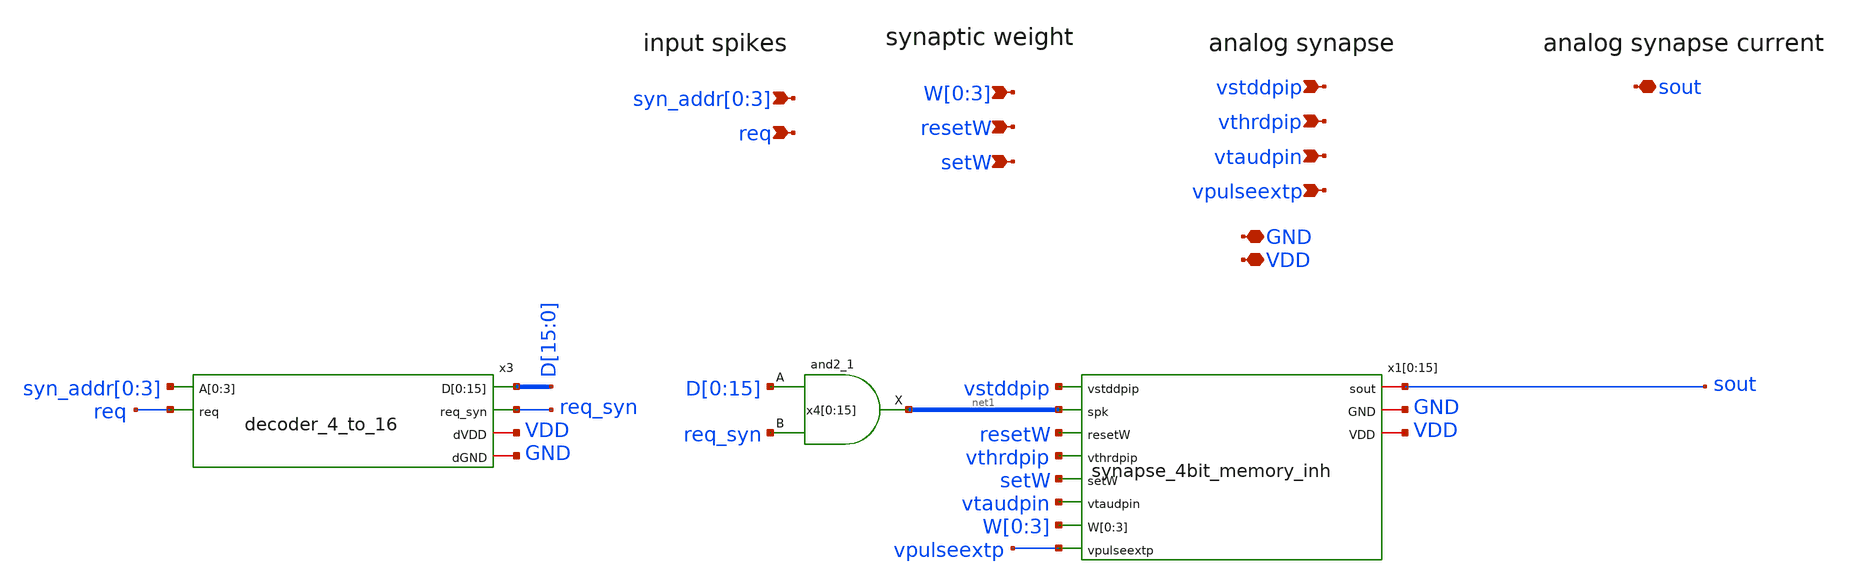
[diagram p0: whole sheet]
** sch_path: design/xschem/synapse_array_programmable_inh_16_to_sout.sch
**.subckt synapse_array_programmable_inh_16_to_sout GND VDD vpulseextp
*+ syn_addr[0],syn_addr[1],syn_addr[2],syn_addr[3] W[0],W[1],W[2],W[3] vthrdpip vtaudpin vstddpip sout setW resetW req
*.iopin GND
*.iopin VDD
*.ipin vpulseextp
*.ipin syn_addr[0],syn_addr[1],syn_addr[2],syn_addr[3]
*.ipin W[0],W[1],W[2],W[3]
*.ipin vthrdpip
*.ipin vtaudpin
*.ipin vstddpip
*.iopin sout
*.ipin setW
*.ipin resetW
*.ipin req
x3 syn_addr[0] syn_addr[1] syn_addr[2] syn_addr[3] D[15] D[14] D[13] D[12] D[11] D[10] D[9] D[8]
+ D[7] D[6] D[5] D[4] D[3] D[2] D[1] D[0] req req_syn VDD GND decoder_4_to_16
x4[0] D[0] req_syn GND GND VDD VDD net1[15] sky130_fd_sc_hd__and2_1
x4[1] D[1] req_syn GND GND VDD VDD net1[14] sky130_fd_sc_hd__and2_1
x4[2] D[2] req_syn GND GND VDD VDD net1[13] sky130_fd_sc_hd__and2_1
x4[3] D[3] req_syn GND GND VDD VDD net1[12] sky130_fd_sc_hd__and2_1
x4[4] D[4] req_syn GND GND VDD VDD net1[11] sky130_fd_sc_hd__and2_1
x4[5] D[5] req_syn GND GND VDD VDD net1[10] sky130_fd_sc_hd__and2_1
x4[6] D[6] req_syn GND GND VDD VDD net1[9] sky130_fd_sc_hd__and2_1
x4[7] D[7] req_syn GND GND VDD VDD net1[8] sky130_fd_sc_hd__and2_1
x4[8] D[8] req_syn GND GND VDD VDD net1[7] sky130_fd_sc_hd__and2_1
x4[9] D[9] req_syn GND GND VDD VDD net1[6] sky130_fd_sc_hd__and2_1
x4[10] D[10] req_syn GND GND VDD VDD net1[5] sky130_fd_sc_hd__and2_1
x4[11] D[11] req_syn GND GND VDD VDD net1[4] sky130_fd_sc_hd__and2_1
x4[12] D[12] req_syn GND GND VDD VDD net1[3] sky130_fd_sc_hd__and2_1
x4[13] D[13] req_syn GND GND VDD VDD net1[2] sky130_fd_sc_hd__and2_1
x4[14] D[14] req_syn GND GND VDD VDD net1[1] sky130_fd_sc_hd__and2_1
x4[15] D[15] req_syn GND GND VDD VDD net1[0] sky130_fd_sc_hd__and2_1
x1[0] sout vstddpip net1[15] resetW vthrdpip setW vtaudpin W[0] W[1] W[2] W[3] vpulseextp GND VDD
+ synapse_4bit_memory_inh
x1[1] sout vstddpip net1[14] resetW vthrdpip setW vtaudpin W[0] W[1] W[2] W[3] vpulseextp GND VDD
+ synapse_4bit_memory_inh
x1[2] sout vstddpip net1[13] resetW vthrdpip setW vtaudpin W[0] W[1] W[2] W[3] vpulseextp GND VDD
+ synapse_4bit_memory_inh
x1[3] sout vstddpip net1[12] resetW vthrdpip setW vtaudpin W[0] W[1] W[2] W[3] vpulseextp GND VDD
+ synapse_4bit_memory_inh
x1[4] sout vstddpip net1[11] resetW vthrdpip setW vtaudpin W[0] W[1] W[2] W[3] vpulseextp GND VDD
+ synapse_4bit_memory_inh
x1[5] sout vstddpip net1[10] resetW vthrdpip setW vtaudpin W[0] W[1] W[2] W[3] vpulseextp GND VDD
+ synapse_4bit_memory_inh
x1[6] sout vstddpip net1[9] resetW vthrdpip setW vtaudpin W[0] W[1] W[2] W[3] vpulseextp GND VDD
+ synapse_4bit_memory_inh
x1[7] sout vstddpip net1[8] resetW vthrdpip setW vtaudpin W[0] W[1] W[2] W[3] vpulseextp GND VDD
+ synapse_4bit_memory_inh
x1[8] sout vstddpip net1[7] resetW vthrdpip setW vtaudpin W[0] W[1] W[2] W[3] vpulseextp GND VDD
+ synapse_4bit_memory_inh
x1[9] sout vstddpip net1[6] resetW vthrdpip setW vtaudpin W[0] W[1] W[2] W[3] vpulseextp GND VDD
+ synapse_4bit_memory_inh
x1[10] sout vstddpip net1[5] resetW vthrdpip setW vtaudpin W[0] W[1] W[2] W[3] vpulseextp GND VDD
+ synapse_4bit_memory_inh
x1[11] sout vstddpip net1[4] resetW vthrdpip setW vtaudpin W[0] W[1] W[2] W[3] vpulseextp GND VDD
+ synapse_4bit_memory_inh
x1[12] sout vstddpip net1[3] resetW vthrdpip setW vtaudpin W[0] W[1] W[2] W[3] vpulseextp GND VDD
+ synapse_4bit_memory_inh
x1[13] sout vstddpip net1[2] resetW vthrdpip setW vtaudpin W[0] W[1] W[2] W[3] vpulseextp GND VDD
+ synapse_4bit_memory_inh
x1[14] sout vstddpip net1[1] resetW vthrdpip setW vtaudpin W[0] W[1] W[2] W[3] vpulseextp GND VDD
+ synapse_4bit_memory_inh
x1[15] sout vstddpip net1[0] resetW vthrdpip setW vtaudpin W[0] W[1] W[2] W[3] vpulseextp GND VDD
+ synapse_4bit_memory_inh
**.ends

* expanding   symbol:  decoder_4_to_16.sym # of pins=6
** sym_path: design/xschem/decoder_4_to_16.sym
** sch_path: design/xschem/decoder_4_to_16.sch
.subckt decoder_4_to_16 A[0] A[1] A[2] A[3] D[0] D[1] D[2] D[3] D[4] D[5] D[6] D[7] D[8] D[9] D[10]
+ D[11] D[12] D[13] D[14] D[15] req req_syn dVDD dGND
*.ipin A[0],A[1],A[2],A[3]
*.ipin req
*.opin D[0],D[1],D[2],D[3],D[4],D[5],D[6],D[7],D[8],D[9],D[10],D[11],D[12],D[13],D[14],D[15]
*.opin req_syn
*.iopin dVDD
*.iopin dGND
x21 req dGND dGND dVDD dVDD net5 sky130_fd_sc_hd__inv_1
x22 net5 dGND dGND dVDD dVDD net6 sky130_fd_sc_hd__inv_1
x23 net6 dGND dGND dVDD dVDD net7 sky130_fd_sc_hd__inv_1
x24 net7 dGND dGND dVDD dVDD req_syn sky130_fd_sc_hd__inv_1
x20 A[3] A[2] A[1] A[0] dGND dGND dVDD dVDD D[15] sky130_fd_sc_hd__and4_1
x19 A[3] A[2] A[1] net4 dGND dGND dVDD dVDD D[14] sky130_fd_sc_hd__and4_1
x18 A[3] A[2] net3 A[0] dGND dGND dVDD dVDD D[13] sky130_fd_sc_hd__and4_1
x17 A[3] A[2] net3 net4 dGND dGND dVDD dVDD D[12] sky130_fd_sc_hd__and4_1
x16 A[3] net2 A[1] A[0] dGND dGND dVDD dVDD D[11] sky130_fd_sc_hd__and4_1
x15 A[3] net2 A[1] net4 dGND dGND dVDD dVDD D[10] sky130_fd_sc_hd__and4_1
x13 A[3] net2 net3 A[0] dGND dGND dVDD dVDD D[9] sky130_fd_sc_hd__and4_1
x4 A[3] net2 net3 net4 dGND dGND dVDD dVDD D[8] sky130_fd_sc_hd__and4_1
x5 net1 A[2] A[1] A[0] dGND dGND dVDD dVDD D[7] sky130_fd_sc_hd__and4_1
x6 net1 A[2] A[1] net4 dGND dGND dVDD dVDD D[6] sky130_fd_sc_hd__and4_1
x8 net1 A[2] net3 net4 dGND dGND dVDD dVDD D[4] sky130_fd_sc_hd__and4_1
x9 net1 net2 A[1] net4 dGND dGND dVDD dVDD D[2] sky130_fd_sc_hd__and4_1
x10 net1 net2 net3 net4 dGND dGND dVDD dVDD D[0] sky130_fd_sc_hd__and4_1
x11 net1 net2 net3 A[0] dGND dGND dVDD dVDD D[1] sky130_fd_sc_hd__and4_1
x12 net1 net2 A[1] A[0] dGND dGND dVDD dVDD D[3] sky130_fd_sc_hd__and4_1
x14 net1 A[2] net3 A[0] dGND dGND dVDD dVDD D[5] sky130_fd_sc_hd__and4_1
x1 A[3] dGND dGND dVDD dVDD net1 sky130_fd_sc_hd__inv_4
x2 A[2] dGND dGND dVDD dVDD net2 sky130_fd_sc_hd__inv_4
x3 A[1] dGND dGND dVDD dVDD net3 sky130_fd_sc_hd__inv_4
x7 A[0] dGND dGND dVDD dVDD net4 sky130_fd_sc_hd__inv_4
.ends


* expanding   symbol:  synapse_4bit_memory_inh.sym # of pins=11
** sym_path: design/xschem/synapse_4bit_memory_inh.sym
** sch_path: design/xschem/synapse_4bit_memory_inh.sch
.subckt synapse_4bit_memory_inh sout vstddpip spk resetW vthrdpip setW vtaudpin W[0] W[1] W[2] W[3]
+ vpulseextp GND VDD
*.iopin GND
*.iopin VDD
*.ipin vpulseextp
*.ipin spk
*.ipin vthrdpip
*.ipin vtaudpin
*.ipin vstddpip
*.ipin W[0],W[1],W[2],W[3]
*.ipin setW
*.ipin resetW
*.iopin sout
x1 vpulseextp spk GND spke VDD spike_extender
x11 resetW GND GND VDD VDD net1 sky130_fd_sc_hd__inv_1
x3 vstddpip net2 net2 net2 net2 spke sout vthrdpip vtaudpin GND VDD dpi_syn_inh_4bit_fc
x2 setW W[0] net1 GND GND VDD VDD net3 net2 sky130_fd_sc_hd__dfrbp_1
.ends


* expanding   symbol:  spike_extender.sym # of pins=5
** sym_path: design/xschem/spike_extender.sym
** sch_path: design/xschem/spike_extender.sch
.subckt spike_extender vpulseextp spk GND spkext VDD
*.iopin GND
*.iopin VDD
*.ipin spk
*.opin spkext
*.ipin vpulseextp
XM1 net1 spk GND GND sky130_fd_pr__nfet_01v8 L=0.15 W=0.65 nf=1 ad='int((nf+1)/2) * W/nf * 0.29' as='int((nf+2)/2) * W/nf * 0.29'
+ pd='2*int((nf+1)/2) * (W/nf + 0.29)' ps='2*int((nf+2)/2) * (W/nf + 0.29)' nrd='0.29 / W' nrs='0.29 / W'
+ sa=0 sb=0 sd=0 mult=1 m=1
XM6 net1 vpulseextp VDD VDD sky130_fd_pr__pfet_01v8 L=2 W=1 nf=1 ad='int((nf+1)/2) * W/nf * 0.29' as='int((nf+2)/2) * W/nf * 0.29'
+ pd='2*int((nf+1)/2) * (W/nf + 0.29)' ps='2*int((nf+2)/2) * (W/nf + 0.29)' nrd='0.29 / W' nrs='0.29 / W'
+ sa=0 sb=0 sd=0 mult=1 m=1
XM5 net3 net2 GND GND sky130_fd_pr__nfet_01v8 L=0.15 W=0.65 nf=1 ad='int((nf+1)/2) * W/nf * 0.29' as='int((nf+2)/2) * W/nf * 0.29'
+ pd='2*int((nf+1)/2) * (W/nf + 0.29)' ps='2*int((nf+2)/2) * (W/nf + 0.29)' nrd='0.29 / W' nrs='0.29 / W'
+ sa=0 sb=0 sd=0 mult=1 m=1
XM8 spkext net3 GND GND sky130_fd_pr__nfet_01v8 L=0.15 W=0.65 nf=1 ad='int((nf+1)/2) * W/nf * 0.29' as='int((nf+2)/2) * W/nf * 0.29'
+ pd='2*int((nf+1)/2) * (W/nf + 0.29)' ps='2*int((nf+2)/2) * (W/nf + 0.29)' nrd='0.29 / W' nrs='0.29 / W'
+ sa=0 sb=0 sd=0 mult=1 m=1
XM4 net3 net2 VDD VDD sky130_fd_pr__pfet_01v8 L=0.15 W=1.0 nf=1 ad='int((nf+1)/2) * W/nf * 0.29' as='int((nf+2)/2) * W/nf * 0.29'
+ pd='2*int((nf+1)/2) * (W/nf + 0.29)' ps='2*int((nf+2)/2) * (W/nf + 0.29)' nrd='0.29 / W' nrs='0.29 / W'
+ sa=0 sb=0 sd=0 mult=1 m=1
XM7 spkext net3 VDD VDD sky130_fd_pr__pfet_01v8 L=0.15 W=1.0 nf=1 ad='int((nf+1)/2) * W/nf * 0.29' as='int((nf+2)/2) * W/nf * 0.29'
+ pd='2*int((nf+1)/2) * (W/nf + 0.29)' ps='2*int((nf+2)/2) * (W/nf + 0.29)' nrd='0.29 / W' nrs='0.29 / W'
+ sa=0 sb=0 sd=0 mult=1 m=1
XM2 net2 net1 GND GND sky130_fd_pr__nfet_01v8 L=0.15 W=0.65 nf=1 ad='int((nf+1)/2) * W/nf * 0.29' as='int((nf+2)/2) * W/nf * 0.29'
+ pd='2*int((nf+1)/2) * (W/nf + 0.29)' ps='2*int((nf+2)/2) * (W/nf + 0.29)' nrd='0.29 / W' nrs='0.29 / W'
+ sa=0 sb=0 sd=0 mult=1 m=1
XM3 net2 net1 VDD VDD sky130_fd_pr__pfet_01v8 L=0.15 W=1.0 nf=1 ad='int((nf+1)/2) * W/nf * 0.29' as='int((nf+2)/2) * W/nf * 0.29'
+ pd='2*int((nf+1)/2) * (W/nf + 0.29)' ps='2*int((nf+2)/2) * (W/nf + 0.29)' nrd='0.29 / W' nrs='0.29 / W'
+ sa=0 sb=0 sd=0 mult=1 m=1
XM9 GND net1 GND GND sky130_fd_pr__nfet_01v8 L=1 W=0.65 nf=1 ad='int((nf+1)/2) * W/nf * 0.29' as='int((nf+2)/2) * W/nf * 0.29'
+ pd='2*int((nf+1)/2) * (W/nf + 0.29)' ps='2*int((nf+2)/2) * (W/nf + 0.29)' nrd='0.29 / W' nrs='0.29 / W'
+ sa=0 sb=0 sd=0 mult=1 m=1
.ends


* expanding   symbol:  dpi_syn_inh_4bit_fc.sym # of pins=8
** sym_path: design/xschem/dpi_syn_inh_4bit_fc.sym
** sch_path: design/xschem/dpi_syn_inh_4bit_fc.sch
.subckt dpi_syn_inh_4bit_fc vstdp weight_b[0] weight_b[1] weight_b[2] weight_b[3] spk sout vthrdp
+ vtaun GND VDD
*.ipin spk
*.iopin vstdp
*.iopin vthrdp
*.iopin vtaun
*.iopin sout
*.iopin GND
*.iopin VDD
*.ipin weight_b[0],weight_b[1],weight_b[2],weight_b[3]
XM5 net2 net3 net1 VDD sky130_fd_pr__pfet_01v8 L=0.2 W=1.2 nf=1 ad='int((nf+1)/2) * W/nf * 0.29' as='int((nf+2)/2) * W/nf * 0.29'
+ pd='2*int((nf+1)/2) * (W/nf + 0.29)' ps='2*int((nf+2)/2) * (W/nf + 0.29)' nrd='0.29 / W' nrs='0.29 / W'
+ sa=0 sb=0 sd=0 mult=1 m=1
XM2 GND vthrdp net2 VDD sky130_fd_pr__pfet_01v8 L=0.2 W=1.2 nf=1 ad='int((nf+1)/2) * W/nf * 0.29' as='int((nf+2)/2) * W/nf * 0.29'
+ pd='2*int((nf+1)/2) * (W/nf + 0.29)' ps='2*int((nf+2)/2) * (W/nf + 0.29)' nrd='0.29 / W' nrs='0.29 / W'
+ sa=0 sb=0 sd=0 mult=1 m=1
XM3 vsin vsin net2 VDD sky130_fd_pr__pfet_01v8 L=0.2 W=1.2 nf=1 ad='int((nf+1)/2) * W/nf * 0.29' as='int((nf+2)/2) * W/nf * 0.29'
+ pd='2*int((nf+1)/2) * (W/nf + 0.29)' ps='2*int((nf+2)/2) * (W/nf + 0.29)' nrd='0.29 / W' nrs='0.29 / W'
+ sa=0 sb=0 sd=0 mult=1 m=1
XM4 vsin vtaun GND GND sky130_fd_pr__nfet_01v8 L=0.25 W=0.8 nf=1 ad='int((nf+1)/2) * W/nf * 0.29' as='int((nf+2)/2) * W/nf * 0.29'
+ pd='2*int((nf+1)/2) * (W/nf + 0.29)' ps='2*int((nf+2)/2) * (W/nf + 0.29)' nrd='0.29 / W' nrs='0.29 / W'
+ sa=0 sb=0 sd=0 mult=1 m=1
XM6 sout vsin net8 GND sky130_fd_pr__nfet_01v8 L=0.25 W=0.8 nf=1 ad='int((nf+1)/2) * W/nf * 0.29' as='int((nf+2)/2) * W/nf * 0.29'
+ pd='2*int((nf+1)/2) * (W/nf + 0.29)' ps='2*int((nf+2)/2) * (W/nf + 0.29)' nrd='0.29 / W' nrs='0.29 / W'
+ sa=0 sb=0 sd=0 mult=1 m=1
XM7 net3 spk GND GND sky130_fd_pr__nfet_01v8 L=0.25 W=0.8 nf=1 ad='int((nf+1)/2) * W/nf * 0.29' as='int((nf+2)/2) * W/nf * 0.29'
+ pd='2*int((nf+1)/2) * (W/nf + 0.29)' ps='2*int((nf+2)/2) * (W/nf + 0.29)' nrd='0.29 / W' nrs='0.29 / W'
+ sa=0 sb=0 sd=0 mult=1 m=1
XM8 net3 spk VDD VDD sky130_fd_pr__pfet_01v8 L=0.2 W=1.2 nf=1 ad='int((nf+1)/2) * W/nf * 0.29' as='int((nf+2)/2) * W/nf * 0.29'
+ pd='2*int((nf+1)/2) * (W/nf + 0.29)' ps='2*int((nf+2)/2) * (W/nf + 0.29)' nrd='0.29 / W' nrs='0.29 / W'
+ sa=0 sb=0 sd=0 mult=1 m=1
XC1 GND vsin sky130_fd_pr__cap_mim_m3_1 W=5 L=5 MF=1 m=1
XM9 net4 vstdp VDD VDD sky130_fd_pr__pfet_01v8 L=0.4 W=1.2 nf=1 ad='int((nf+1)/2) * W/nf * 0.29' as='int((nf+2)/2) * W/nf * 0.29'
+ pd='2*int((nf+1)/2) * (W/nf + 0.29)' ps='2*int((nf+2)/2) * (W/nf + 0.29)' nrd='0.29 / W' nrs='0.29 / W'
+ sa=0 sb=0 sd=0 mult=1 m=1
XM10 net1 weight_b[0] net4 VDD sky130_fd_pr__pfet_01v8 L=0.2 W=1.2 nf=1 ad='int((nf+1)/2) * W/nf * 0.29'
+ as='int((nf+2)/2) * W/nf * 0.29' pd='2*int((nf+1)/2) * (W/nf + 0.29)' ps='2*int((nf+2)/2) * (W/nf + 0.29)'
+ nrd='0.29 / W' nrs='0.29 / W' sa=0 sb=0 sd=0 mult=1 m=1
XM11 net1 weight_b[1] net5 VDD sky130_fd_pr__pfet_01v8 L=0.2 W=1.2 nf=1 ad='int((nf+1)/2) * W/nf * 0.29'
+ as='int((nf+2)/2) * W/nf * 0.29' pd='2*int((nf+1)/2) * (W/nf + 0.29)' ps='2*int((nf+2)/2) * (W/nf + 0.29)'
+ nrd='0.29 / W' nrs='0.29 / W' sa=0 sb=0 sd=0 mult=1 m=1
XM1 net5 vstdp VDD VDD sky130_fd_pr__pfet_01v8 L=1.5 W=1.2 nf=1 ad='int((nf+1)/2) * W/nf * 0.29' as='int((nf+2)/2) * W/nf * 0.29'
+ pd='2*int((nf+1)/2) * (W/nf + 0.29)' ps='2*int((nf+2)/2) * (W/nf + 0.29)' nrd='0.29 / W' nrs='0.29 / W'
+ sa=0 sb=0 sd=0 mult=1 m=1
XM12 net6 vstdp VDD VDD sky130_fd_pr__pfet_01v8 L=3.0 W=1.2 nf=1 ad='int((nf+1)/2) * W/nf * 0.29' as='int((nf+2)/2) * W/nf * 0.29'
+ pd='2*int((nf+1)/2) * (W/nf + 0.29)' ps='2*int((nf+2)/2) * (W/nf + 0.29)' nrd='0.29 / W' nrs='0.29 / W'
+ sa=0 sb=0 sd=0 mult=1 m=1
XM13 net7 vstdp VDD VDD sky130_fd_pr__pfet_01v8 L=6.0 W=1.2 nf=1 ad='int((nf+1)/2) * W/nf * 0.29' as='int((nf+2)/2) * W/nf * 0.29'
+ pd='2*int((nf+1)/2) * (W/nf + 0.29)' ps='2*int((nf+2)/2) * (W/nf + 0.29)' nrd='0.29 / W' nrs='0.29 / W'
+ sa=0 sb=0 sd=0 mult=1 m=1
XM14 net1 weight_b[2] net6 VDD sky130_fd_pr__pfet_01v8 L=0.2 W=1.2 nf=1 ad='int((nf+1)/2) * W/nf * 0.29'
+ as='int((nf+2)/2) * W/nf * 0.29' pd='2*int((nf+1)/2) * (W/nf + 0.29)' ps='2*int((nf+2)/2) * (W/nf + 0.29)'
+ nrd='0.29 / W' nrs='0.29 / W' sa=0 sb=0 sd=0 mult=1 m=1
XM15 net1 weight_b[3] net7 VDD sky130_fd_pr__pfet_01v8 L=0.2 W=1.2 nf=1 ad='int((nf+1)/2) * W/nf * 0.29'
+ as='int((nf+2)/2) * W/nf * 0.29' pd='2*int((nf+1)/2) * (W/nf + 0.29)' ps='2*int((nf+2)/2) * (W/nf + 0.29)'
+ nrd='0.29 / W' nrs='0.29 / W' sa=0 sb=0 sd=0 mult=1 m=1
Vmeas net8 GND 0
.save i(vmeas)
.ends

.end
